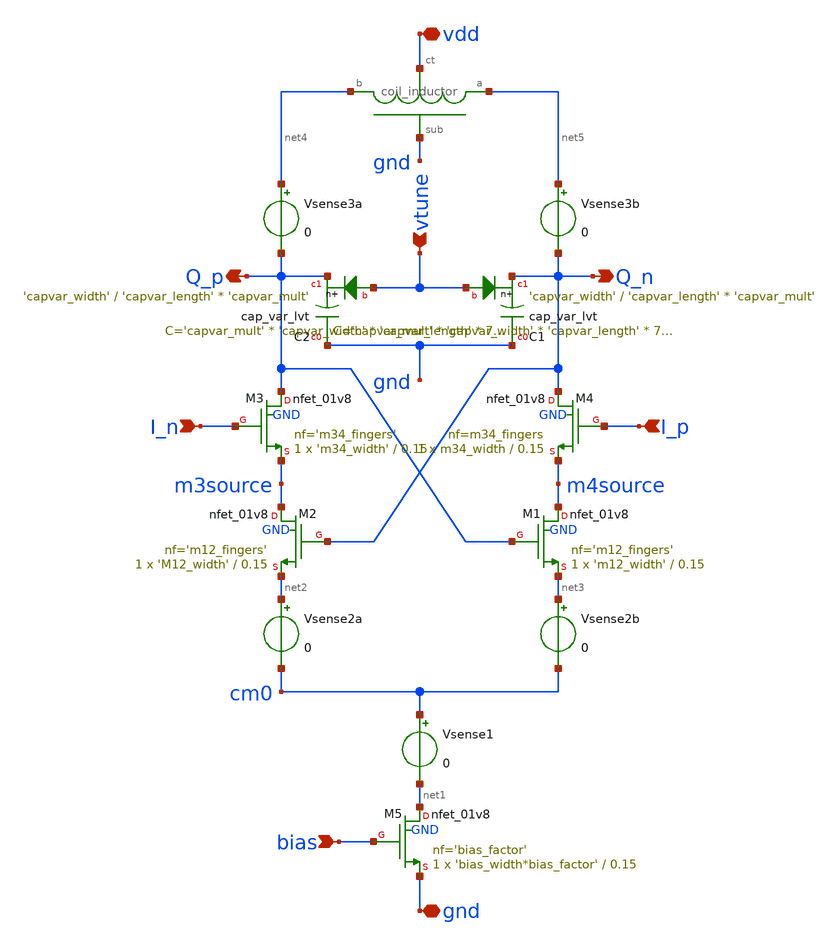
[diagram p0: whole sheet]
** sch_path: xschem/half_qvco_param.sch
**.subckt half_qvco_param vdd gnd I_n bias Q_p Q_n I_p vtune
*.iopin vdd
*.iopin gnd
*.ipin I_n
*.ipin bias
*.opin Q_p
*.opin Q_n
*.ipin I_p
*.ipin vtune
XM1 m4source Q_p net3 GND sky130_fd_pr__nfet_01v8 L=0.15 W='m12_width' nf='m12_fingers' ad='int((nf+1)/2) * W/nf * 0.29'
+ as='int((nf+2)/2) * W/nf * 0.29' pd='2*int((nf+1)/2) * (W/nf + 0.29)' ps='2*int((nf+2)/2) * (W/nf + 0.29)'
+ nrd='0.29 / W' nrs='0.29 / W' sa=0 sb=0 sd=0 mult=1 m=1
XM2 m3source Q_n net2 GND sky130_fd_pr__nfet_01v8 L=0.15 W='M12_width' nf='m12_fingers' ad='int((nf+1)/2) * W/nf * 0.29'
+ as='int((nf+2)/2) * W/nf * 0.29' pd='2*int((nf+1)/2) * (W/nf + 0.29)' ps='2*int((nf+2)/2) * (W/nf + 0.29)'
+ nrd='0.29 / W' nrs='0.29 / W' sa=0 sb=0 sd=0 mult=1 m=1
XC1 gnd Q_n vtune sky130_fd_pr__cap_var_lvt W='capvar_width' L='capvar_length' VM='capvar_mult' m='capvar_mult'
XC2 gnd Q_p vtune sky130_fd_pr__cap_var_lvt W='capvar_width' L='capvar_length' VM='capvar_mult' m='capvar_mult'
XM5 net1 bias gnd GND sky130_fd_pr__nfet_01v8 L=0.15 W='bias_width*bias_factor' nf='bias_factor' ad='int((nf+1)/2) * W/nf * 0.29'
+ as='int((nf+2)/2) * W/nf * 0.29' pd='2*int((nf+1)/2) * (W/nf + 0.29)' ps='2*int((nf+2)/2) * (W/nf + 0.29)'
+ nrd='0.29 / W' nrs='0.29 / W' sa=0 sb=0 sd=0 mult=1 m=1
XM3 Q_p I_n m3source GND sky130_fd_pr__nfet_01v8 L=0.15 W='m34_width' nf='m34_fingers' ad='int((nf+1)/2) * W/nf * 0.29'
+ as='int((nf+2)/2) * W/nf * 0.29' pd='2*int((nf+1)/2) * (W/nf + 0.29)' ps='2*int((nf+2)/2) * (W/nf + 0.29)'
+ nrd='0.29 / W' nrs='0.29 / W' sa=0 sb=0 sd=0 mult=1 m=1
XM4 Q_n I_p m4source GND sky130_fd_pr__nfet_01v8 L=0.15 W=m34_width nf=m34_fingers ad='int((nf+1)/2) * W/nf * 0.29'
+ as='int((nf+2)/2) * W/nf * 0.29' pd='2*int((nf+1)/2) * (W/nf + 0.29)' ps='2*int((nf+2)/2) * (W/nf + 0.29)'
+ nrd='0.29 / W' nrs='0.29 / W' sa=0 sb=0 sd=0 mult=1 m=1
Vsense1 cm0 net1 0
Vsense2a net2 cm0 0
Vsense2b net3 cm0 0
Vsense3b net5 Q_n 0
Vsense3a net4 Q_p 0
XL1 net5 net4 vdd gnd sky130_fd_pr__ind_03_90
**.ends
.end
